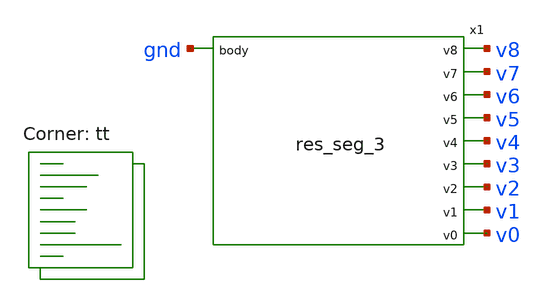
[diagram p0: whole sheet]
** sch_path: xschem/res_seg_3-tb.sch
**.subckt res_seg_3-tb
x1 v8 v7 v6 v5 v4 v3 v2 v1 v0 gnd res_seg_3
**** begin user architecture code



  .param max_freq=500e3 period={1/max_freq} time_high={period/2}
  .param delay_vin1={time_high} delay_vin2={time_high*1.5}
  .param lval=100u

  .option wnflag=1
  .option safecurrents

  V8 v8 gnd dc 4.2113
  v0 v0 gnd dc 3.8451
  *Vin  in  gnd pulse(0 1.8 {delay_vin1} 1p 1p {time_high} {period})
  *Vinb inb gnd pulse(1.8 0 {delay_vin1} 1p 1p {time_high} {period})

  .control
     reset
     save all
     tran 0.1n 100n
     write res_segment.raw
     set appendwrite

     *reset
     *save all
     *dc vref 0 1.8 0.1
     *write lvsf-tb.raw
*    quit 0
  .endc



.lib $::SKYWATER_MODELS/sky130.lib.spice tt
**** end user architecture code
**.ends

* expanding   symbol:  res_seg_3.sym # of pins=10
** sym_path: xschem/res_seg_3.sym
** sch_path: xschem/res_seg_3.sch
.subckt res_seg_3 v8 v7 v6 v5 v4 v3 v2 v1 v0 body
*.opin v8
*.opin v7
*.opin v6
*.opin v5
*.opin v4
*.opin v3
*.opin v2
*.opin v1
*.opin v0
*.ipin body
XR1 v7 v8 body sky130_fd_pr__res_xhigh_po_0p35 L=0.9486 mult=1 m=1
XR2 v6 v7 body sky130_fd_pr__res_xhigh_po_0p35 L=0.8888 mult=1 m=1
XR3 v5 v6 body sky130_fd_pr__res_xhigh_po_0p35 L=0.8460 mult=1 m=1
XR4 v4 v5 body sky130_fd_pr__res_xhigh_po_0p35 L=0.8118 mult=1 m=1
XR5 v3 v4 body sky130_fd_pr__res_xhigh_po_0p35 L=0.7691 mult=1 m=1
XR6 v2 v3 body sky130_fd_pr__res_xhigh_po_0p35 L=0.7349 mult=1 m=1
XR7 v1 v2 body sky130_fd_pr__res_xhigh_po_0p35 L=0.7178 mult=1 m=1
XR8 v0 v1 body sky130_fd_pr__res_xhigh_po_0p35 L=0.6922 mult=1 m=1
.ends

.end
